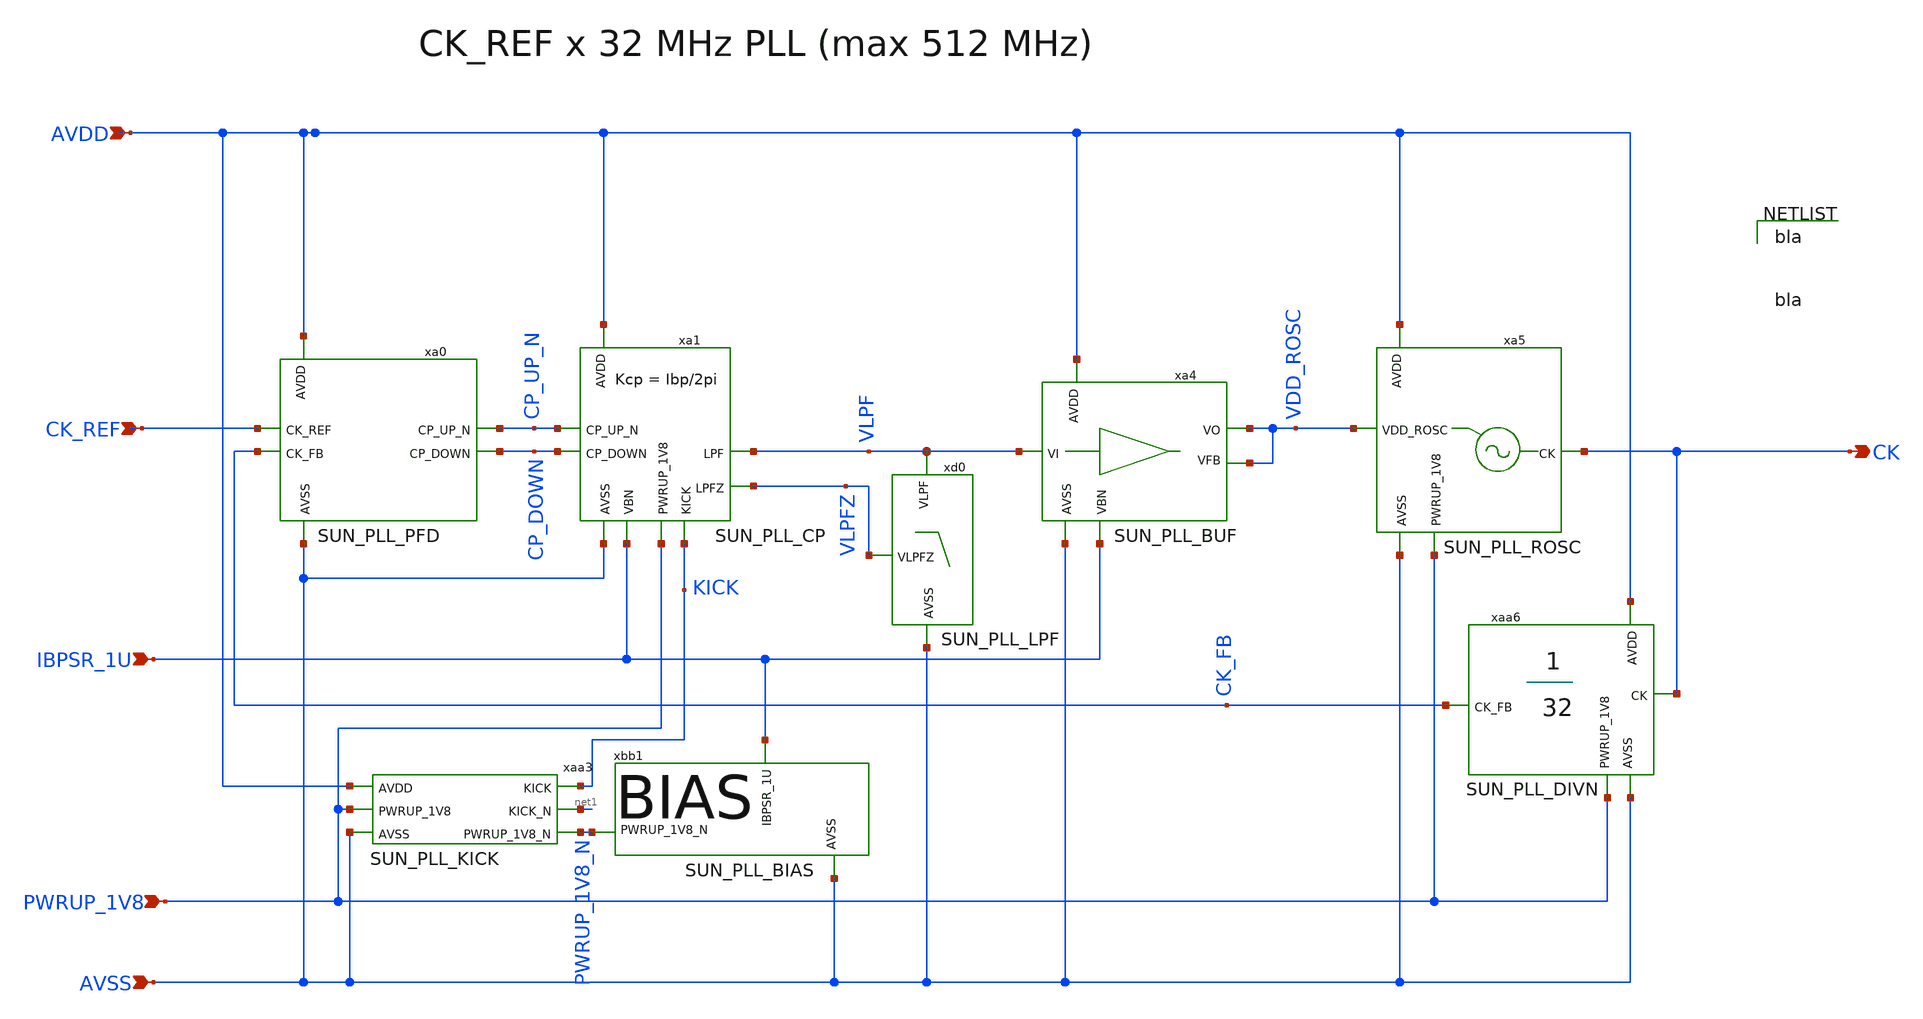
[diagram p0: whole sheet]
** sch_path: design/SUN_PLL_SKY130NM/SUN_PLL.sch
**.subckt SUN_PLL AVDD AVSS PWRUP_1V8 CK_REF CK IBPSR_1U
*.ipin AVDD
*.ipin AVSS
*.ipin PWRUP_1V8
*.ipin CK_REF
*.opin CK
*.ipin IBPSR_1U
xa5 AVDD CK VDD_ROSC PWRUP_1V8 AVSS SUN_PLL_ROSC
xaa6 AVDD CK_FB CK PWRUP_1V8 AVSS SUN_PLL_DIVN
xbb1 IBPSR_1U PWRUP_1V8_N AVSS SUN_PLL_BIAS
xa4 AVDD VDD_ROSC VLPF VDD_ROSC IBPSR_1U AVSS SUN_PLL_BUF
xd0 VLPFZ AVSS VLPF SUN_PLL_LPF
xa1 AVDD CP_UP_N VLPF CP_DOWN IBPSR_1U AVSS VLPFZ PWRUP_1V8 KICK SUN_PLL_CP
xa0 AVDD CP_UP_N CK_REF CP_DOWN CK_FB AVSS SUN_PLL_PFD
xaa3 AVDD KICK net1 PWRUP_1V8 AVSS PWRUP_1V8_N SUN_PLL_KICK
**** begin user architecture code

bla


bla

**** end user architecture code
**.ends
.end
